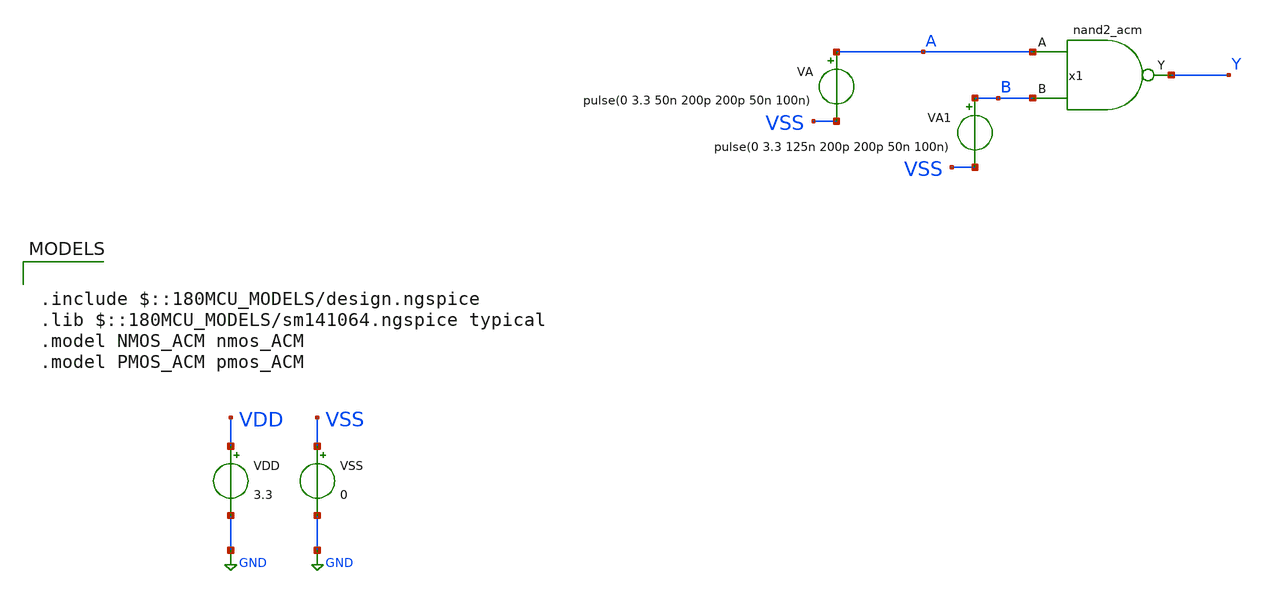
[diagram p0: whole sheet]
** sch_path: legacy/Examples/GF180MCU/xschem/TB_nand2_acm.sch
**.subckt TB_nand2_acm
x1 A B Y VDD VSS nand2_acm
VA A VSS pulse(0 3.3 50n 200p 200p 50n 100n)
VDD VDD GND 3.3
VSS VSS GND 0
VA1 B VSS pulse(0 3.3 125n 200p 200p 50n 100n)
**** begin user architecture code

.include $::180MCU_MODELS/design.ngspice
.lib $::180MCU_MODELS/sm141064.ngspice typical
.model NMOS_ACM nmos_ACM
.model PMOS_ACM pmos_ACM



.option gmin=1e-15

.control
pre_osdi ./NMOS_ACM_2V0.osdi
pre_osdi ./PMOS_ACM_2V0.osdi
save all


tran 1n 500n
remzerovec
write TB_nand2_acm.raw
set appendwrite

.endc


**** end user architecture code
**.ends
.GLOBAL GND
.end
